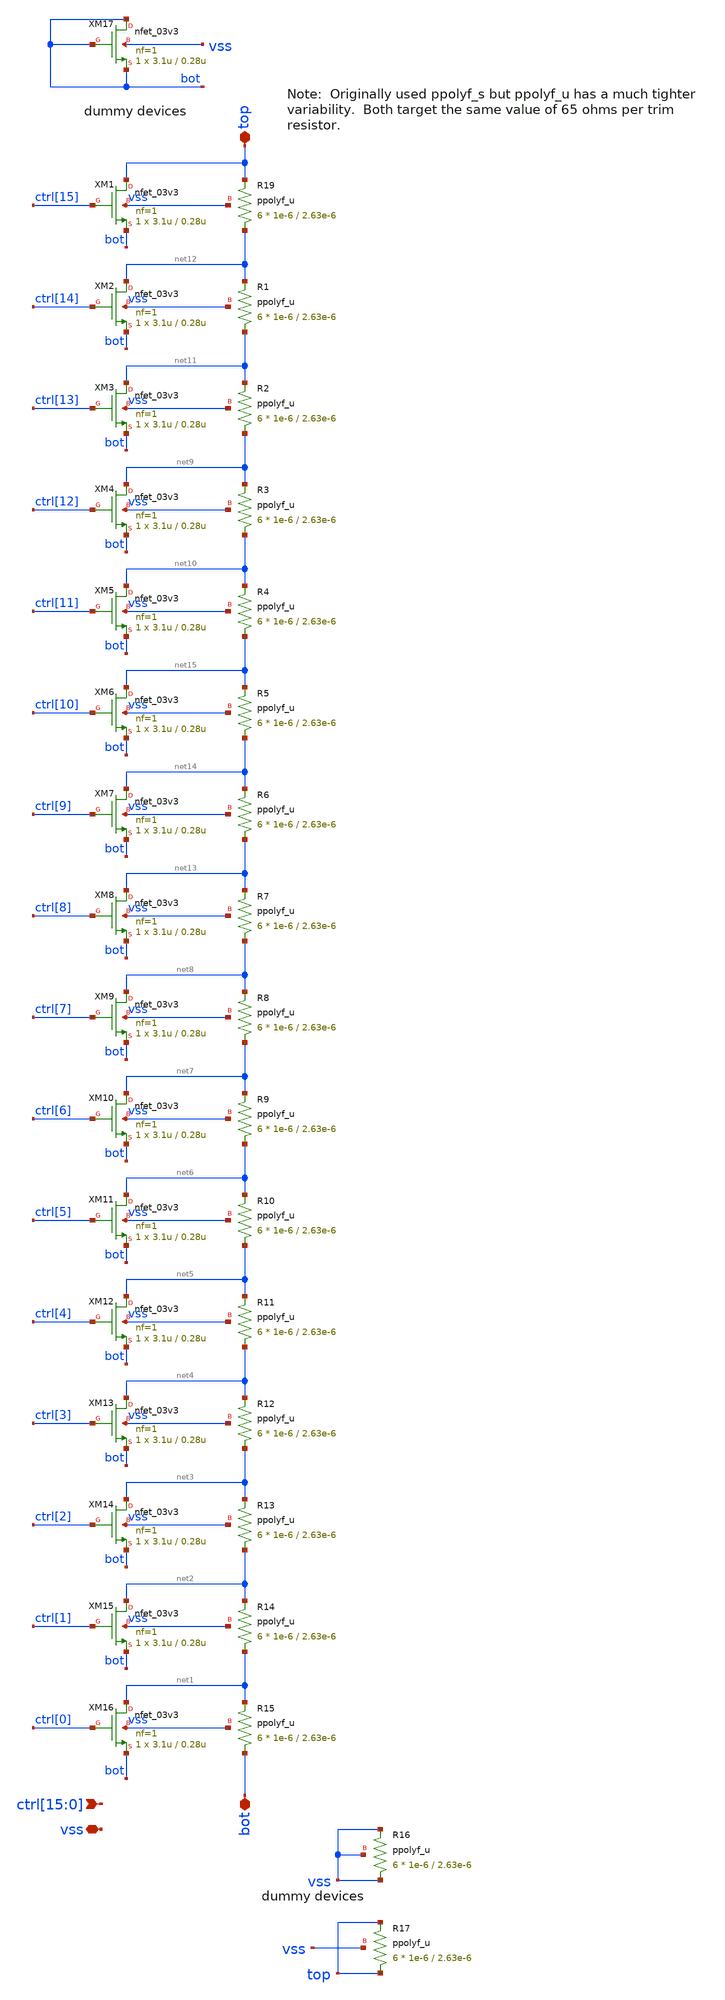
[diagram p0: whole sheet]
** sch_path: projects/programmable_transceiver_platform/analog/core_support/bandgap/xschem/bg_trim.sch
**.subckt bg_trim vss
*+ ctrl[15],ctrl[14],ctrl[13],ctrl[12],ctrl[11],ctrl[10],ctrl[9],ctrl[8],ctrl[7],ctrl[6],ctrl[5],ctrl[4],ctrl[3],ctrl[2],ctrl[1],ctrl[0] bot top
*.iopin vss
*.ipin
*+ ctrl[15],ctrl[14],ctrl[13],ctrl[12],ctrl[11],ctrl[10],ctrl[9],ctrl[8],ctrl[7],ctrl[6],ctrl[5],ctrl[4],ctrl[3],ctrl[2],ctrl[1],ctrl[0]
*.iopin bot
*.iopin top
XM1 top ctrl[15] bot vss nfet_03v3 L=0.28u W=3.1u nf=1 ad='int((nf+1)/2) * W/nf * 0.18u' as='int((nf+2)/2) * W/nf * 0.18u'
+ pd='2*int((nf+1)/2) * (W/nf + 0.18u)' ps='2*int((nf+2)/2) * (W/nf + 0.18u)' nrd='0.18u / W' nrs='0.18u / W'
+ sa=0 sb=0 sd=0 m=1 par=1
XR19 net12 top vss ppolyf_u r_width=1e-6 r_length=2.63e-6 m=6
XM17 bot bot bot vss nfet_03v3 L=0.28u W=3.1u nf=1 ad='int((nf+1)/2) * W/nf * 0.18u' as='int((nf+2)/2) * W/nf * 0.18u'
+ pd='2*int((nf+1)/2) * (W/nf + 0.18u)' ps='2*int((nf+2)/2) * (W/nf + 0.18u)' nrd='0.18u / W' nrs='0.18u / W'
+ sa=0 sb=0 sd=0 m=1 par=1
XM2 net12 ctrl[14] bot vss nfet_03v3 L=0.28u W=3.1u nf=1 ad='int((nf+1)/2) * W/nf * 0.18u' as='int((nf+2)/2) * W/nf * 0.18u'
+ pd='2*int((nf+1)/2) * (W/nf + 0.18u)' ps='2*int((nf+2)/2) * (W/nf + 0.18u)' nrd='0.18u / W' nrs='0.18u / W'
+ sa=0 sb=0 sd=0 m=1 par=1
XM3 net11 ctrl[13] bot vss nfet_03v3 L=0.28u W=3.1u nf=1 ad='int((nf+1)/2) * W/nf * 0.18u' as='int((nf+2)/2) * W/nf * 0.18u'
+ pd='2*int((nf+1)/2) * (W/nf + 0.18u)' ps='2*int((nf+2)/2) * (W/nf + 0.18u)' nrd='0.18u / W' nrs='0.18u / W'
+ sa=0 sb=0 sd=0 m=1 par=1
XR1 net11 net12 vss ppolyf_u r_width=1e-6 r_length=2.63e-6 m=6
XR2 net9 net11 vss ppolyf_u r_width=1e-6 r_length=2.63e-6 m=6
XR3 net10 net9 vss ppolyf_u r_width=1e-6 r_length=2.63e-6 m=6
XR4 net15 net10 vss ppolyf_u r_width=1e-6 r_length=2.63e-6 m=6
XR5 net14 net15 vss ppolyf_u r_width=1e-6 r_length=2.63e-6 m=6
XR6 net13 net14 vss ppolyf_u r_width=1e-6 r_length=2.63e-6 m=6
XR7 net8 net13 vss ppolyf_u r_width=1e-6 r_length=2.63e-6 m=6
XR8 net7 net8 vss ppolyf_u r_width=1e-6 r_length=2.63e-6 m=6
XR9 net6 net7 vss ppolyf_u r_width=1e-6 r_length=2.63e-6 m=6
XR10 net5 net6 vss ppolyf_u r_width=1e-6 r_length=2.63e-6 m=6
XR11 net4 net5 vss ppolyf_u r_width=1e-6 r_length=2.63e-6 m=6
XR12 net3 net4 vss ppolyf_u r_width=1e-6 r_length=2.63e-6 m=6
XR13 net2 net3 vss ppolyf_u r_width=1e-6 r_length=2.63e-6 m=6
XR14 net1 net2 vss ppolyf_u r_width=1e-6 r_length=2.63e-6 m=6
XR15 bot net1 vss ppolyf_u r_width=1e-6 r_length=2.63e-6 m=6
XR16 vss vss vss ppolyf_u r_width=1e-6 r_length=2.63e-6 m=6
XR17 top top vss ppolyf_u r_width=1e-6 r_length=2.63e-6 m=6
XM4 net9 ctrl[12] bot vss nfet_03v3 L=0.28u W=3.1u nf=1 ad='int((nf+1)/2) * W/nf * 0.18u' as='int((nf+2)/2) * W/nf * 0.18u'
+ pd='2*int((nf+1)/2) * (W/nf + 0.18u)' ps='2*int((nf+2)/2) * (W/nf + 0.18u)' nrd='0.18u / W' nrs='0.18u / W'
+ sa=0 sb=0 sd=0 m=1 par=1
XM5 net10 ctrl[11] bot vss nfet_03v3 L=0.28u W=3.1u nf=1 ad='int((nf+1)/2) * W/nf * 0.18u' as='int((nf+2)/2) * W/nf * 0.18u'
+ pd='2*int((nf+1)/2) * (W/nf + 0.18u)' ps='2*int((nf+2)/2) * (W/nf + 0.18u)' nrd='0.18u / W' nrs='0.18u / W'
+ sa=0 sb=0 sd=0 m=1 par=1
XM6 net15 ctrl[10] bot vss nfet_03v3 L=0.28u W=3.1u nf=1 ad='int((nf+1)/2) * W/nf * 0.18u' as='int((nf+2)/2) * W/nf * 0.18u'
+ pd='2*int((nf+1)/2) * (W/nf + 0.18u)' ps='2*int((nf+2)/2) * (W/nf + 0.18u)' nrd='0.18u / W' nrs='0.18u / W'
+ sa=0 sb=0 sd=0 m=1 par=1
XM7 net14 ctrl[9] bot vss nfet_03v3 L=0.28u W=3.1u nf=1 ad='int((nf+1)/2) * W/nf * 0.18u' as='int((nf+2)/2) * W/nf * 0.18u'
+ pd='2*int((nf+1)/2) * (W/nf + 0.18u)' ps='2*int((nf+2)/2) * (W/nf + 0.18u)' nrd='0.18u / W' nrs='0.18u / W'
+ sa=0 sb=0 sd=0 m=1 par=1
XM8 net13 ctrl[8] bot vss nfet_03v3 L=0.28u W=3.1u nf=1 ad='int((nf+1)/2) * W/nf * 0.18u' as='int((nf+2)/2) * W/nf * 0.18u'
+ pd='2*int((nf+1)/2) * (W/nf + 0.18u)' ps='2*int((nf+2)/2) * (W/nf + 0.18u)' nrd='0.18u / W' nrs='0.18u / W'
+ sa=0 sb=0 sd=0 m=1 par=1
XM9 net8 ctrl[7] bot vss nfet_03v3 L=0.28u W=3.1u nf=1 ad='int((nf+1)/2) * W/nf * 0.18u' as='int((nf+2)/2) * W/nf * 0.18u'
+ pd='2*int((nf+1)/2) * (W/nf + 0.18u)' ps='2*int((nf+2)/2) * (W/nf + 0.18u)' nrd='0.18u / W' nrs='0.18u / W'
+ sa=0 sb=0 sd=0 m=1 par=1
XM10 net7 ctrl[6] bot vss nfet_03v3 L=0.28u W=3.1u nf=1 ad='int((nf+1)/2) * W/nf * 0.18u' as='int((nf+2)/2) * W/nf * 0.18u'
+ pd='2*int((nf+1)/2) * (W/nf + 0.18u)' ps='2*int((nf+2)/2) * (W/nf + 0.18u)' nrd='0.18u / W' nrs='0.18u / W'
+ sa=0 sb=0 sd=0 m=1 par=1
XM11 net6 ctrl[5] bot vss nfet_03v3 L=0.28u W=3.1u nf=1 ad='int((nf+1)/2) * W/nf * 0.18u' as='int((nf+2)/2) * W/nf * 0.18u'
+ pd='2*int((nf+1)/2) * (W/nf + 0.18u)' ps='2*int((nf+2)/2) * (W/nf + 0.18u)' nrd='0.18u / W' nrs='0.18u / W'
+ sa=0 sb=0 sd=0 m=1 par=1
XM12 net5 ctrl[4] bot vss nfet_03v3 L=0.28u W=3.1u nf=1 ad='int((nf+1)/2) * W/nf * 0.18u' as='int((nf+2)/2) * W/nf * 0.18u'
+ pd='2*int((nf+1)/2) * (W/nf + 0.18u)' ps='2*int((nf+2)/2) * (W/nf + 0.18u)' nrd='0.18u / W' nrs='0.18u / W'
+ sa=0 sb=0 sd=0 m=1 par=1
XM13 net4 ctrl[3] bot vss nfet_03v3 L=0.28u W=3.1u nf=1 ad='int((nf+1)/2) * W/nf * 0.18u' as='int((nf+2)/2) * W/nf * 0.18u'
+ pd='2*int((nf+1)/2) * (W/nf + 0.18u)' ps='2*int((nf+2)/2) * (W/nf + 0.18u)' nrd='0.18u / W' nrs='0.18u / W'
+ sa=0 sb=0 sd=0 m=1 par=1
XM14 net3 ctrl[2] bot vss nfet_03v3 L=0.28u W=3.1u nf=1 ad='int((nf+1)/2) * W/nf * 0.18u' as='int((nf+2)/2) * W/nf * 0.18u'
+ pd='2*int((nf+1)/2) * (W/nf + 0.18u)' ps='2*int((nf+2)/2) * (W/nf + 0.18u)' nrd='0.18u / W' nrs='0.18u / W'
+ sa=0 sb=0 sd=0 m=1 par=1
XM15 net2 ctrl[1] bot vss nfet_03v3 L=0.28u W=3.1u nf=1 ad='int((nf+1)/2) * W/nf * 0.18u' as='int((nf+2)/2) * W/nf * 0.18u'
+ pd='2*int((nf+1)/2) * (W/nf + 0.18u)' ps='2*int((nf+2)/2) * (W/nf + 0.18u)' nrd='0.18u / W' nrs='0.18u / W'
+ sa=0 sb=0 sd=0 m=1 par=1
XM16 net1 ctrl[0] bot vss nfet_03v3 L=0.28u W=3.1u nf=1 ad='int((nf+1)/2) * W/nf * 0.18u' as='int((nf+2)/2) * W/nf * 0.18u'
+ pd='2*int((nf+1)/2) * (W/nf + 0.18u)' ps='2*int((nf+2)/2) * (W/nf + 0.18u)' nrd='0.18u / W' nrs='0.18u / W'
+ sa=0 sb=0 sd=0 m=1 par=1
**.ends
.end
